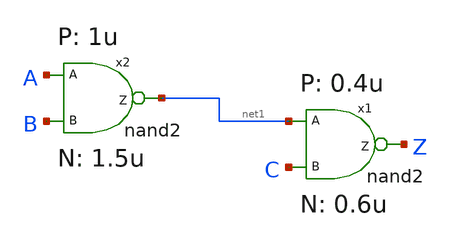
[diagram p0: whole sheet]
** sch_path: xschem_library/mylib/test2.sch
**.subckt test2
x1 Z net1 C nand2 WP=12u LP=0.4u WN=8u LN=0.6u
x2 net1 A B nand2 WP=5u LP=1u WN=3u LN=1.5u
**.ends

* expanding   symbol:  mylib/nand2.sym # of pins=3
** sym_path: library/mylib/nand2.sym
** sch_path: library/mylib/nand2.sch
.subckt nand2 Z A B  WP=8u LP=0.18u WN=5u LN=0.18u
*.ipin A
*.opin Z
*.ipin B
m1 Z A net1 VSS nmos w=WN l=LN m=1
m2 Z B VCC VCC pmos w=WP l=LP m=1
m3 Z A VCC VCC pmos w=WP l=LP m=1
m4 net1 B VSS VSS nmos w=WN l=LN m=1
.ends

.GLOBAL VCC
.GLOBAL VSS
.end
